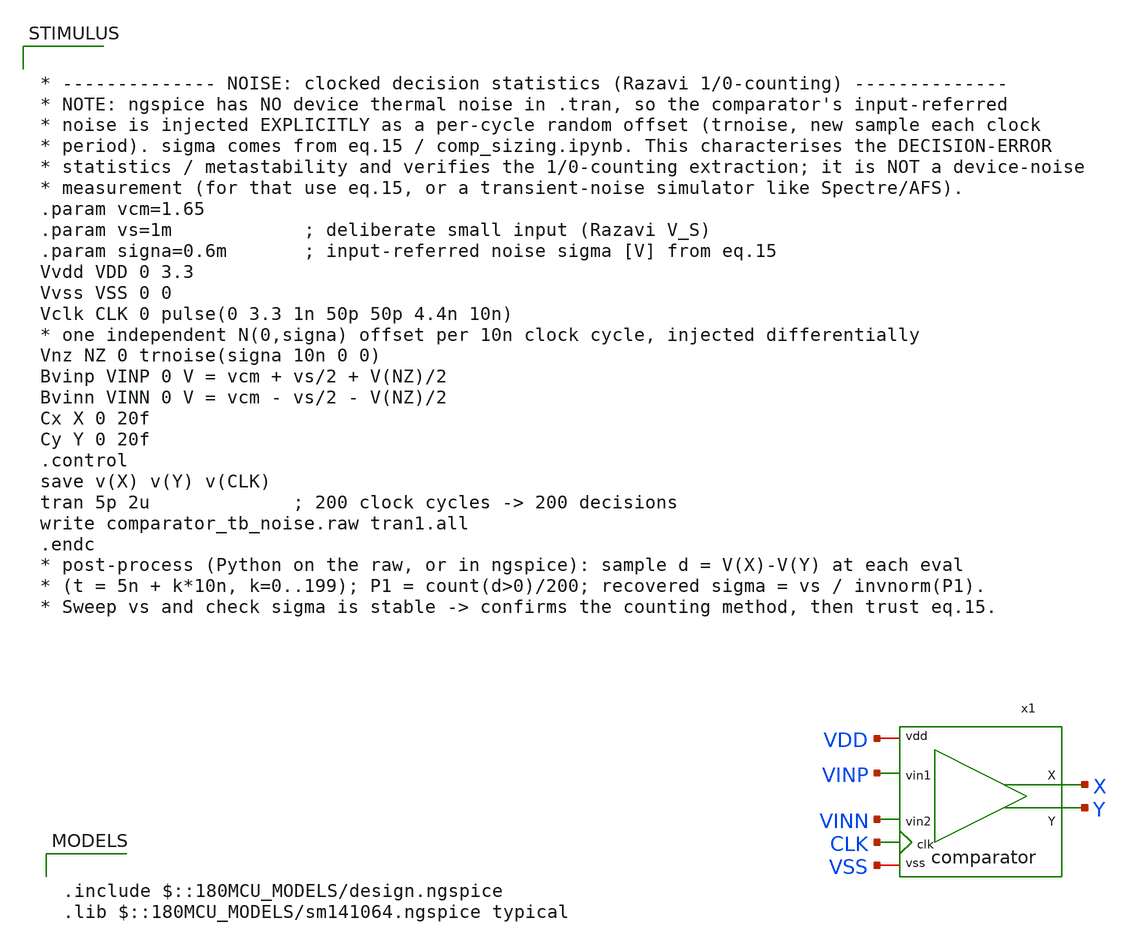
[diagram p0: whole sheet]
** sch_path: designs/libs/core_analog/saradc/tb/comparator_tb_noise.sch
**.subckt comparator_tb_noise
x1 VDD VSS X VINP Y VINN CLK comparator
**** begin user architecture code

.include $::180MCU_MODELS/design.ngspice
.lib $::180MCU_MODELS/sm141064.ngspice typical



* -------------- NOISE: clocked decision statistics (Razavi 1/0-counting) --------------
* NOTE: ngspice has NO device thermal noise in .tran, so the comparator's input-referred
* noise is injected EXPLICITLY as a per-cycle random offset (trnoise, new sample each clock
* period). sigma comes from eq.15 / comp_sizing.ipynb. This characterises the DECISION-ERROR
* statistics / metastability and verifies the 1/0-counting extraction; it is NOT a device-noise
* measurement (for that use eq.15, or a transient-noise simulator like Spectre/AFS).
.param vcm=1.65
.param vs=1m            ; deliberate small input (Razavi V_S)
.param signa=0.6m       ; input-referred noise sigma [V] from eq.15
Vvdd VDD 0 3.3
Vvss VSS 0 0
Vclk CLK 0 pulse(0 3.3 1n 50p 50p 4.4n 10n)
* one independent N(0,signa) offset per 10n clock cycle, injected differentially
Vnz NZ 0 trnoise(signa 10n 0 0)
Bvinp VINP 0 V = vcm + vs/2 + V(NZ)/2
Bvinn VINN 0 V = vcm - vs/2 - V(NZ)/2
Cx X 0 20f
Cy Y 0 20f
.control
save v(X) v(Y) v(CLK)
tran 5p 2u             ; 200 clock cycles -> 200 decisions
write comparator_tb_noise.raw tran1.all
.endc
* post-process (Python on the raw, or in ngspice): sample d = V(X)-V(Y) at each eval
* (t = 5n + k*10n, k=0..199); P1 = count(d>0)/200; recovered sigma = vs / invnorm(P1).
* Sweep vs and check sigma is stable -> confirms the counting method, then trust eq.15.


**** end user architecture code
**.ends

* expanding   symbol:  comparator.sym # of pins=7
** sym_path: designs/libs/core_analog/saradc/comparator.sym
** sch_path: designs/libs/core_analog/saradc/comparator.sch
.subckt comparator vdd vss X vin1 Y vin2 clk
*.iopin vdd
*.iopin vss
*.ipin vin1
*.ipin vin2
*.ipin clk
*.opin X
*.opin Y
XM1 P vin1 net1 vss nfet_03v3 L=0.5u W=4u nf=4 ad='int((nf+1)/2) * W/nf * 0.18u' as='int((nf+2)/2) *
+ W/nf * 0.18u' pd='2*int((nf+1)/2) * (W/nf + 0.18u)' ps='2*int((nf+2)/2) * (W/nf + 0.18u)' nrd='0.18u
+ / W' nrs='0.18u / W' sa=0 sb=0 sd=0 m=1
XM2 Q vin2 net1 vss nfet_03v3 L=0.5u W=4u nf=4 ad='int((nf+1)/2) * W/nf * 0.18u' as='int((nf+2)/2) *
+ W/nf * 0.18u' pd='2*int((nf+1)/2) * (W/nf + 0.18u)' ps='2*int((nf+2)/2) * (W/nf + 0.18u)' nrd='0.18u
+ / W' nrs='0.18u / W' sa=0 sb=0 sd=0 m=1
XM3 X Y P vss nfet_03v3 L=0.28u W=2u nf=2 ad='int((nf+1)/2) * W/nf * 0.18u' as='int((nf+2)/2) * W/nf
+ * 0.18u' pd='2*int((nf+1)/2) * (W/nf + 0.18u)' ps='2*int((nf+2)/2) * (W/nf + 0.18u)' nrd='0.18u / W' nrs='0.18u
+ / W' sa=0 sb=0 sd=0 m=1
XM4 Y X Q vss nfet_03v3 L=0.28u W=2u nf=2 ad='int((nf+1)/2) * W/nf * 0.18u' as='int((nf+2)/2) * W/nf
+ * 0.18u' pd='2*int((nf+1)/2) * (W/nf + 0.18u)' ps='2*int((nf+2)/2) * (W/nf + 0.18u)' nrd='0.18u / W' nrs='0.18u
+ / W' sa=0 sb=0 sd=0 m=1
XM5 X Y vdd vdd pfet_03v3 L=0.28u W=6u nf=2 ad='int((nf+1)/2) * W/nf * 0.18u' as='int((nf+2)/2) * W/nf
+ * 0.18u' pd='2*int((nf+1)/2) * (W/nf + 0.18u)' ps='2*int((nf+2)/2) * (W/nf + 0.18u)' nrd='0.18u / W' nrs='0.18u
+ / W' sa=0 sb=0 sd=0 m=1
XM6 Y X vdd vdd pfet_03v3 L=0.28u W=6u nf=2 ad='int((nf+1)/2) * W/nf * 0.18u' as='int((nf+2)/2) * W/nf
+ * 0.18u' pd='2*int((nf+1)/2) * (W/nf + 0.18u)' ps='2*int((nf+2)/2) * (W/nf + 0.18u)' nrd='0.18u / W' nrs='0.18u
+ / W' sa=0 sb=0 sd=0 m=1
XM7 net1 clk vss vss nfet_03v3 L=0.28u W=6u nf=4 ad='int((nf+1)/2) * W/nf * 0.18u' as='int((nf+2)/2)
+ * W/nf * 0.18u' pd='2*int((nf+1)/2) * (W/nf + 0.18u)' ps='2*int((nf+2)/2) * (W/nf + 0.18u)' nrd='0.18u
+ / W' nrs='0.18u / W' sa=0 sb=0 sd=0 m=1
XM8 X clk vdd vdd pfet_03v3 L=0.28u W=2u nf=1 ad='int((nf+1)/2) * W/nf * 0.18u' as='int((nf+2)/2) * W/nf
+ * 0.18u' pd='2*int((nf+1)/2) * (W/nf + 0.18u)' ps='2*int((nf+2)/2) * (W/nf + 0.18u)' nrd='0.18u / W' nrs='0.18u
+ / W' sa=0 sb=0 sd=0 m=1
XM9 P clk vdd vdd pfet_03v3 L=0.28u W=2u nf=1 ad='int((nf+1)/2) * W/nf * 0.18u' as='int((nf+2)/2) * W/nf
+ * 0.18u' pd='2*int((nf+1)/2) * (W/nf + 0.18u)' ps='2*int((nf+2)/2) * (W/nf + 0.18u)' nrd='0.18u / W' nrs='0.18u
+ / W' sa=0 sb=0 sd=0 m=1
XM10 Y clk vdd vdd pfet_03v3 L=0.28u W=2u nf=1 ad='int((nf+1)/2) * W/nf * 0.18u' as='int((nf+2)/2) *
+ W/nf * 0.18u' pd='2*int((nf+1)/2) * (W/nf + 0.18u)' ps='2*int((nf+2)/2) * (W/nf + 0.18u)' nrd='0.18u
+ / W' nrs='0.18u / W' sa=0 sb=0 sd=0 m=1
XM11 Q clk vdd vdd pfet_03v3 L=0.28u W=2u nf=1 ad='int((nf+1)/2) * W/nf * 0.18u' as='int((nf+2)/2) *
+ W/nf * 0.18u' pd='2*int((nf+1)/2) * (W/nf + 0.18u)' ps='2*int((nf+2)/2) * (W/nf + 0.18u)' nrd='0.18u
+ / W' nrs='0.18u / W' sa=0 sb=0 sd=0 m=1
.ends

.end
